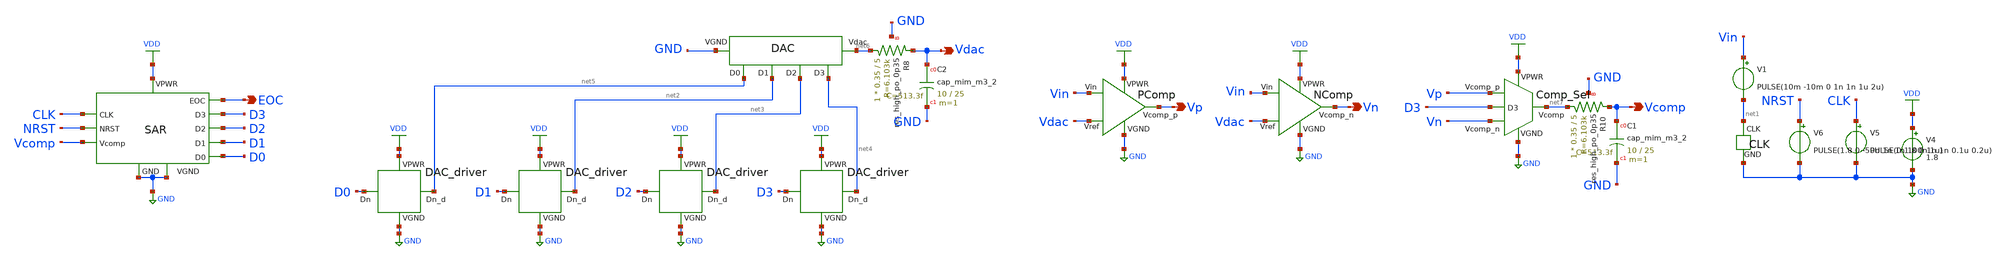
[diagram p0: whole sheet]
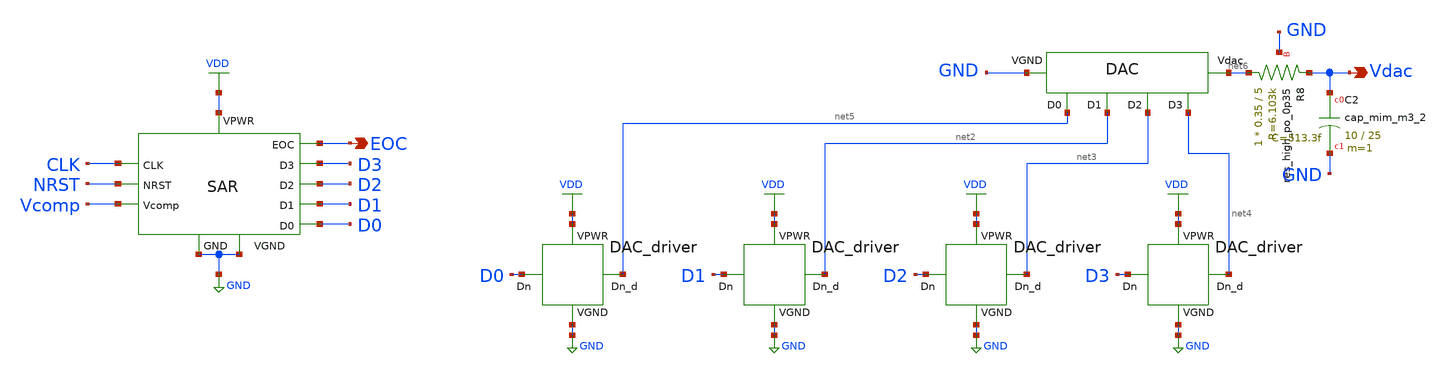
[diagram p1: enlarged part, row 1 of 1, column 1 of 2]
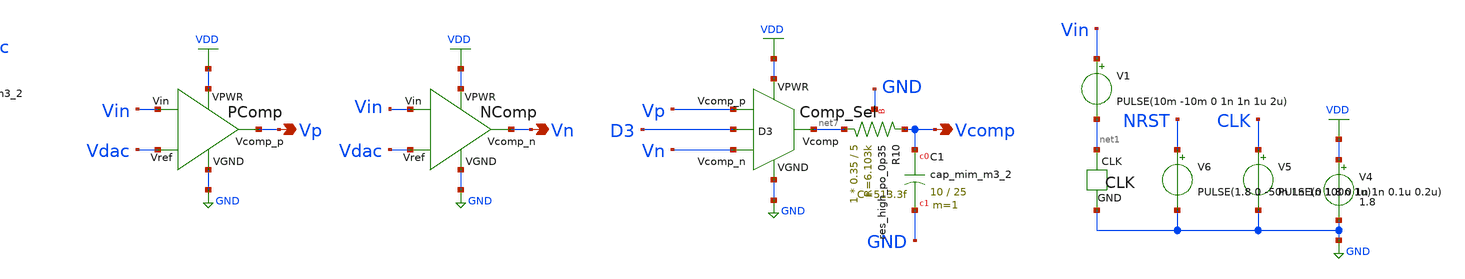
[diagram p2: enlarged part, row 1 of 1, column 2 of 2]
** sch_path: xschem/subckts/ADC.sch
**.subckt ADC Vdac Vcomp EOC Vp Vn
*.opin Vdac
*.opin Vcomp
*.opin EOC
*.opin Vp
*.opin Vn
V4 VDD GND 1.8
V5 CLK GND PULSE(0 1.8 0 1n 1n 0.1u 0.2u)
V6 NRST GND PULSE(1.8 0 -50n 1n 1n 100n 1u)
V1 Vin net1 PULSE(10m -10m 0 1n 1n 1u 2u)
XR8 net6 Vdac GND sky130_fd_pr__res_high_po_0p35 L=5 mult=1 m=1
XC1 Vcomp GND sky130_fd_pr__cap_mim_m3_2 W=10 L=25 MF=1 m=1
XR10 net7 Vcomp GND sky130_fd_pr__res_high_po_0p35 L=5 mult=1 m=1
XC2 Vdac GND sky130_fd_pr__cap_mim_m3_2 W=10 L=25 MF=1 m=1
x11 VDD Vp D3 net7 Vn GND Comp_Sel
x12 VDD net5 D0 GND DAC_driver
x13 VDD net2 D1 GND DAC_driver
x14 VDD net3 D2 GND DAC_driver
x15 VDD net4 D3 GND DAC_driver
x16 VDD Vdac Vin Vp GND PComp
x17 net6 net5 net3 net4 net2 GND DAC
x18 VDD Vdac Vin Vn GND NComp
x19 net1 GND CLK
x1 VDD GND EOC CLK GND NRST Vcomp D2 D1 D3 D0 SAR
**** begin user architecture code

.lib /home/ttuser/pdk/sky130A/libs.tech/ngspice/sky130.lib.spice tt
.include /home/ttuser/pdk/sky130A/libs.ref/sky130_fd_sc_hd/spice/sky130_fd_sc_hd.spice
.include /home/ttuser/Desktop/DAC_layout.spice
.include /home/ttuser/Desktop/DAC_driver_layout.spice
.include /home/ttuser/Desktop/Comp_Sel_layout.spice
.include /home/ttuser/Desktop/NComp_layout.spice
.include /home/ttuser/Desktop/PComp_layout.spice
.include /home/ttuser/Desktop/SAR_layout.spice
.options method=gear
.options maxstep=1n
.tran 0.2n 4u
.save all
.end

**** end user architecture code
**.ends

* expanding   symbol:  /home/ttuser/Desktop/CLK.sym # of pins=2
** sym_path: xschem/subckts/CLK.sym
** sch_path: xschem/subckts/CLK.sch
.subckt CLK CLK GND
*.ipin GND
*.opin CLK
V6 CLK GND PWL (0n 112m 2000n 112m 2001n 225m 4000n 225m 4001n 337m 6000n 337m 6001n 450m 8000n 450m
+ 8001n 562m 10000n 562m 10001n 675m 12000n 675m 12001n 787m 14000n 787m 14001n 900m 16000n 900m 16001n
+ 1012m 18000n 1012m 18001n 1125m 20000n 1125m 20001n 1237m 22000n 1237m 22001n 1350m 24000n 1350m 24001n
+ 1462m 26000n 1462m 26001n 1575m 28000n 1575m 28001n 1687m 30000n 1687m)
.ends

.GLOBAL VDD
.GLOBAL GND
.end
